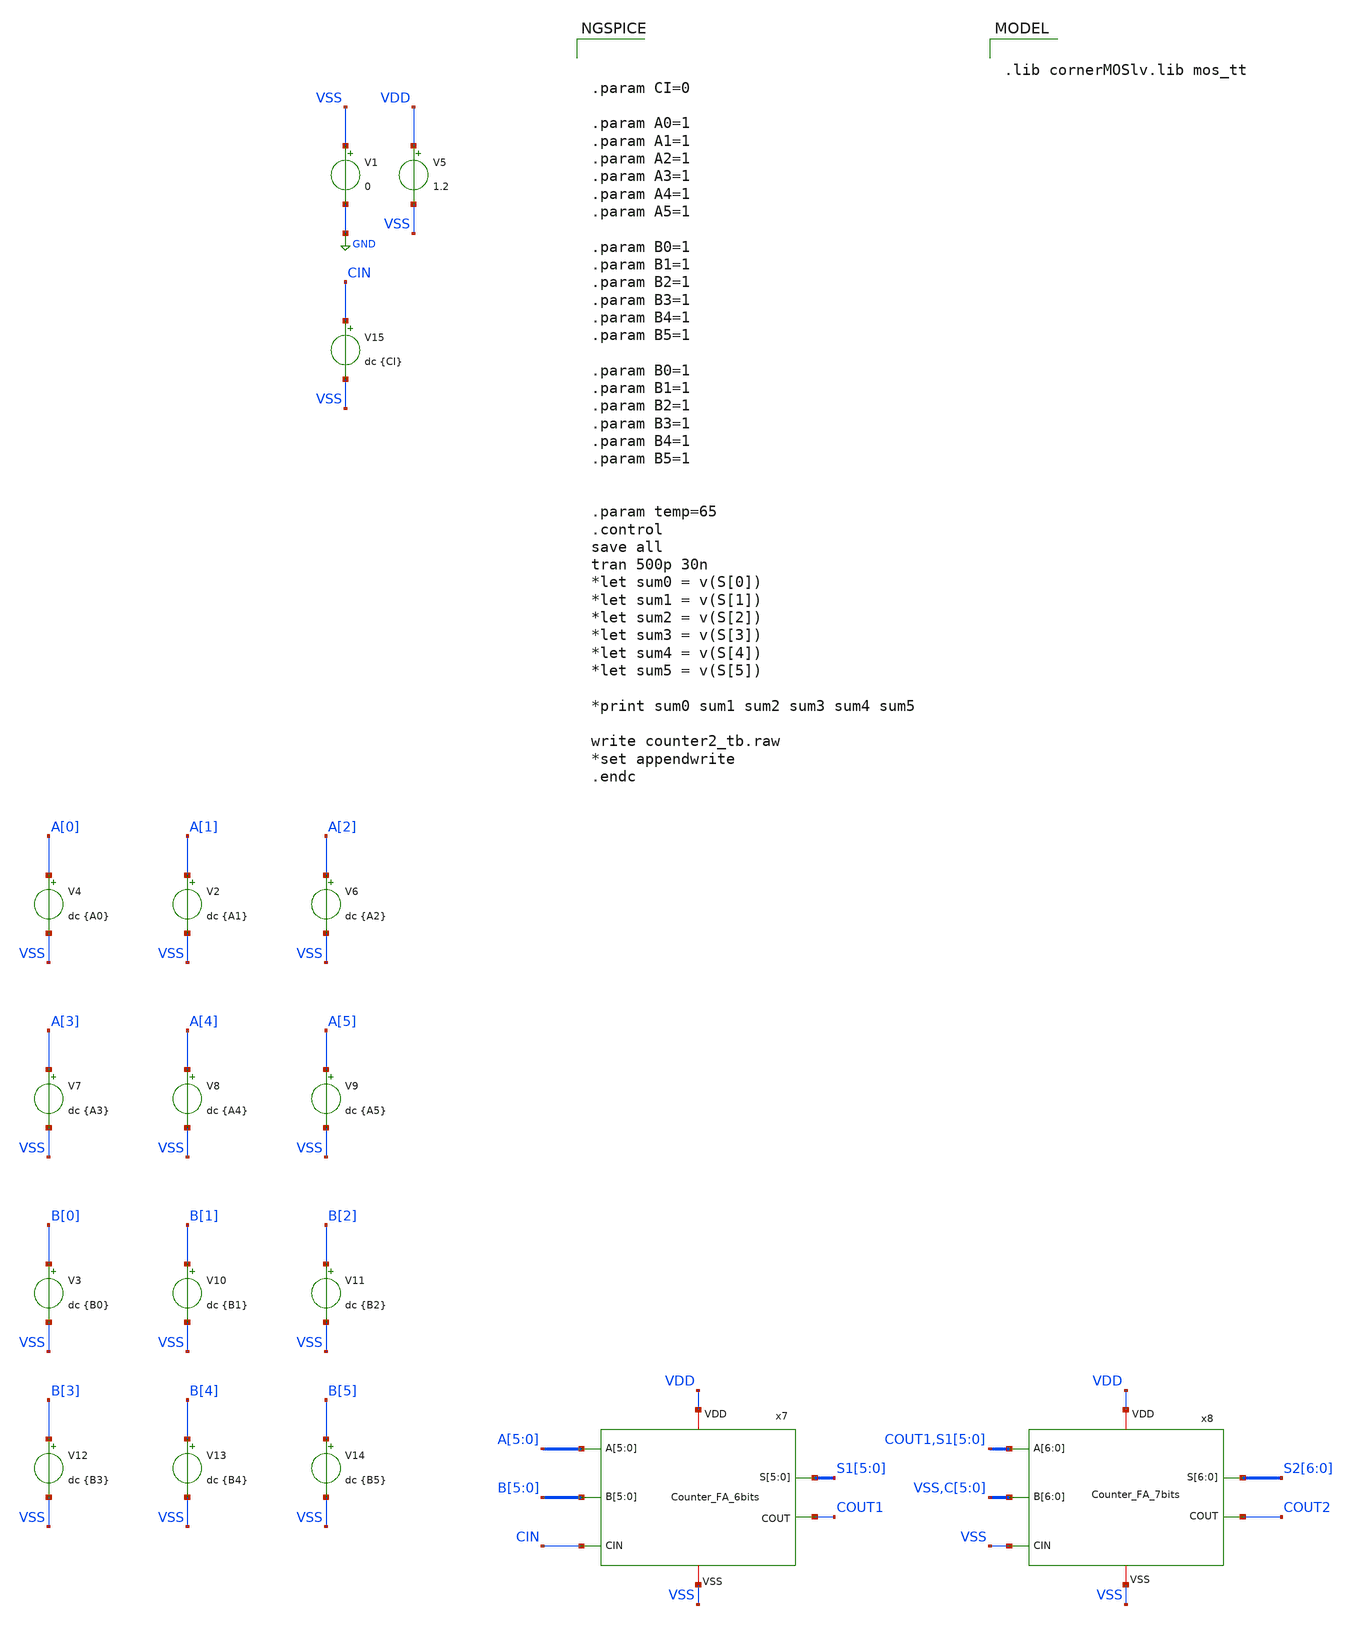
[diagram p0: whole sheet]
** sch_path: ADC8711-main/testbenches/tran/xschem/tb_Counter_FA_7bits.sch
**.subckt tb_Counter_FA_7bits
V1 VSS GND 0
V3 B[0] VSS dc {B0}
V5 VDD VSS 1.2
V4 A[0] VSS dc {A0}
V2 A[1] VSS dc {A1}
V6 A[2] VSS dc {A2}
V7 A[3] VSS dc {A3}
V8 A[4] VSS dc {A4}
V9 A[5] VSS dc {A5}
V10 B[1] VSS dc {B1}
V11 B[2] VSS dc {B2}
V12 B[3] VSS dc {B3}
V13 B[4] VSS dc {B4}
V14 B[5] VSS dc {B5}
V15 CIN VSS dc {CI}
x7 S1[5] S1[4] S1[3] S1[2] S1[1] S1[0] A[5] A[4] A[3] A[2] A[1] A[0] VDD COUT1 B[5] B[4] B[3] B[2]
+ B[1] B[0] VSS CIN Counter_FA_6bits
x8 S2[6] S2[5] S2[4] S2[3] S2[2] S2[1] S2[0] COUT1 S1[5] S1[4] S1[3] S1[2] S1[1] S1[0] VDD COUT2 VSS
+ C[5] C[4] C[3] C[2] C[1] C[0] VSS VSS Counter_FA_7bits
**** begin user architecture code



.param CI=0

.param A0=1
.param A1=1
.param A2=1
.param A3=1
.param A4=1
.param A5=1

.param B0=1
.param B1=1
.param B2=1
.param B3=1
.param B4=1
.param B5=1

.param B0=1
.param B1=1
.param B2=1
.param B3=1
.param B4=1
.param B5=1


.param temp=65
.control
save all
tran 500p 30n
*let sum0 = v(S[0])
*let sum1 = v(S[1])
*let sum2 = v(S[2])
*let sum3 = v(S[3])
*let sum4 = v(S[4])
*let sum5 = v(S[5])

*print sum0 sum1 sum2 sum3 sum4 sum5

write counter2_tb.raw
*set appendwrite
.endc




.lib cornerMOSlv.lib mos_tt

**** end user architecture code
**.ends
.GLOBAL GND
.end
